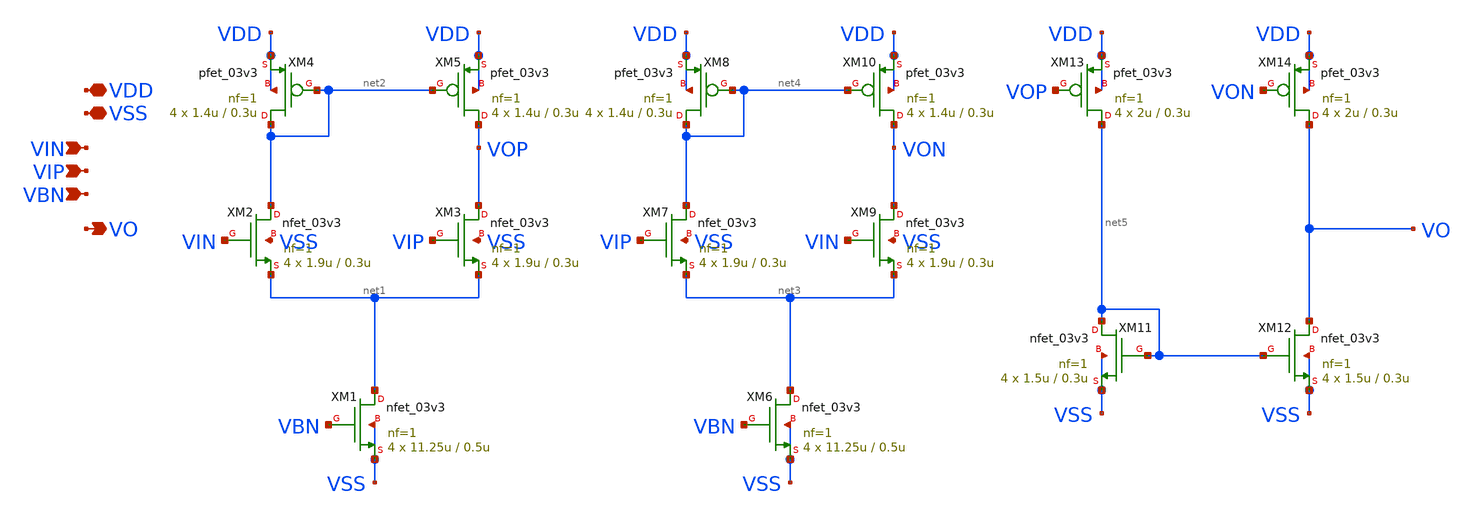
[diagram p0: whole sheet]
** sch_path: designs/libs/core_analog/d2s_converter/d2s_converter.sch
**.subckt d2s_converter VDD VSS VIN VIP VO VBN
*.iopin VDD
*.iopin VSS
*.ipin VIN
*.ipin VIP
*.opin VO
*.ipin VBN
XM2 net2 VIN net1 VSS nfet_03v3 L=0.3u W=1.9u nf=1 ad='int((nf+1)/2) * W/nf * 0.18u' as='int((nf+2)/2) * W/nf * 0.18u'
+ pd='2*int((nf+1)/2) * (W/nf + 0.18u)' ps='2*int((nf+2)/2) * (W/nf + 0.18u)' nrd='0.18u / W' nrs='0.18u / W'
+ sa=0 sb=0 sd=0 m=4
XM4 net2 net2 VDD VDD pfet_03v3 L=0.3u W=1.4u nf=1 ad='int((nf+1)/2) * W/nf * 0.18u' as='int((nf+2)/2) * W/nf * 0.18u'
+ pd='2*int((nf+1)/2) * (W/nf + 0.18u)' ps='2*int((nf+2)/2) * (W/nf + 0.18u)' nrd='0.18u / W' nrs='0.18u / W'
+ sa=0 sb=0 sd=0 m=4
XM11 net5 net5 VSS VSS nfet_03v3 L=0.3u W=1.5u nf=1 ad='int((nf+1)/2) * W/nf * 0.18u' as='int((nf+2)/2) * W/nf * 0.18u'
+ pd='2*int((nf+1)/2) * (W/nf + 0.18u)' ps='2*int((nf+2)/2) * (W/nf + 0.18u)' nrd='0.18u / W' nrs='0.18u / W'
+ sa=0 sb=0 sd=0 m=4
XM13 net5 VOP VDD VDD pfet_03v3 L=0.3u W=2u nf=1 ad='int((nf+1)/2) * W/nf * 0.18u' as='int((nf+2)/2) * W/nf * 0.18u'
+ pd='2*int((nf+1)/2) * (W/nf + 0.18u)' ps='2*int((nf+2)/2) * (W/nf + 0.18u)' nrd='0.18u / W' nrs='0.18u / W'
+ sa=0 sb=0 sd=0 m=4
XM6 net3 VBN VSS VSS nfet_03v3 L=0.5u W=11.25u nf=1 ad='int((nf+1)/2) * W/nf * 0.18u' as='int((nf+2)/2) * W/nf * 0.18u'
+ pd='2*int((nf+1)/2) * (W/nf + 0.18u)' ps='2*int((nf+2)/2) * (W/nf + 0.18u)' nrd='0.18u / W' nrs='0.18u / W'
+ sa=0 sb=0 sd=0 m=4
XM1 net1 VBN VSS VSS nfet_03v3 L=0.5u W=11.25u nf=1 ad='int((nf+1)/2) * W/nf * 0.18u' as='int((nf+2)/2) * W/nf * 0.18u'
+ pd='2*int((nf+1)/2) * (W/nf + 0.18u)' ps='2*int((nf+2)/2) * (W/nf + 0.18u)' nrd='0.18u / W' nrs='0.18u / W'
+ sa=0 sb=0 sd=0 m=4
XM3 VOP VIP net1 VSS nfet_03v3 L=0.3u W=1.9u nf=1 ad='int((nf+1)/2) * W/nf * 0.18u' as='int((nf+2)/2) * W/nf * 0.18u'
+ pd='2*int((nf+1)/2) * (W/nf + 0.18u)' ps='2*int((nf+2)/2) * (W/nf + 0.18u)' nrd='0.18u / W' nrs='0.18u / W'
+ sa=0 sb=0 sd=0 m=4
XM5 VOP net2 VDD VDD pfet_03v3 L=0.3u W=1.4u nf=1 ad='int((nf+1)/2) * W/nf * 0.18u' as='int((nf+2)/2) * W/nf * 0.18u'
+ pd='2*int((nf+1)/2) * (W/nf + 0.18u)' ps='2*int((nf+2)/2) * (W/nf + 0.18u)' nrd='0.18u / W' nrs='0.18u / W'
+ sa=0 sb=0 sd=0 m=4
XM7 net4 VIP net3 VSS nfet_03v3 L=0.3u W=1.9u nf=1 ad='int((nf+1)/2) * W/nf * 0.18u' as='int((nf+2)/2) * W/nf * 0.18u'
+ pd='2*int((nf+1)/2) * (W/nf + 0.18u)' ps='2*int((nf+2)/2) * (W/nf + 0.18u)' nrd='0.18u / W' nrs='0.18u / W'
+ sa=0 sb=0 sd=0 m=4
XM8 net4 net4 VDD VDD pfet_03v3 L=0.3u W=1.4u nf=1 ad='int((nf+1)/2) * W/nf * 0.18u' as='int((nf+2)/2) * W/nf * 0.18u'
+ pd='2*int((nf+1)/2) * (W/nf + 0.18u)' ps='2*int((nf+2)/2) * (W/nf + 0.18u)' nrd='0.18u / W' nrs='0.18u / W'
+ sa=0 sb=0 sd=0 m=4
XM9 VON VIN net3 VSS nfet_03v3 L=0.3u W=1.9u nf=1 ad='int((nf+1)/2) * W/nf * 0.18u' as='int((nf+2)/2) * W/nf * 0.18u'
+ pd='2*int((nf+1)/2) * (W/nf + 0.18u)' ps='2*int((nf+2)/2) * (W/nf + 0.18u)' nrd='0.18u / W' nrs='0.18u / W'
+ sa=0 sb=0 sd=0 m=4
XM10 VON net4 VDD VDD pfet_03v3 L=0.3u W=1.4u nf=1 ad='int((nf+1)/2) * W/nf * 0.18u' as='int((nf+2)/2) * W/nf * 0.18u'
+ pd='2*int((nf+1)/2) * (W/nf + 0.18u)' ps='2*int((nf+2)/2) * (W/nf + 0.18u)' nrd='0.18u / W' nrs='0.18u / W'
+ sa=0 sb=0 sd=0 m=4
XM14 VO VON VDD VDD pfet_03v3 L=0.3u W=2u nf=1 ad='int((nf+1)/2) * W/nf * 0.18u' as='int((nf+2)/2) * W/nf * 0.18u'
+ pd='2*int((nf+1)/2) * (W/nf + 0.18u)' ps='2*int((nf+2)/2) * (W/nf + 0.18u)' nrd='0.18u / W' nrs='0.18u / W'
+ sa=0 sb=0 sd=0 m=4
XM12 VO net5 VSS VSS nfet_03v3 L=0.3u W=1.5u nf=1 ad='int((nf+1)/2) * W/nf * 0.18u' as='int((nf+2)/2) * W/nf * 0.18u'
+ pd='2*int((nf+1)/2) * (W/nf + 0.18u)' ps='2*int((nf+2)/2) * (W/nf + 0.18u)' nrd='0.18u / W' nrs='0.18u / W'
+ sa=0 sb=0 sd=0 m=4
**.ends
.end
